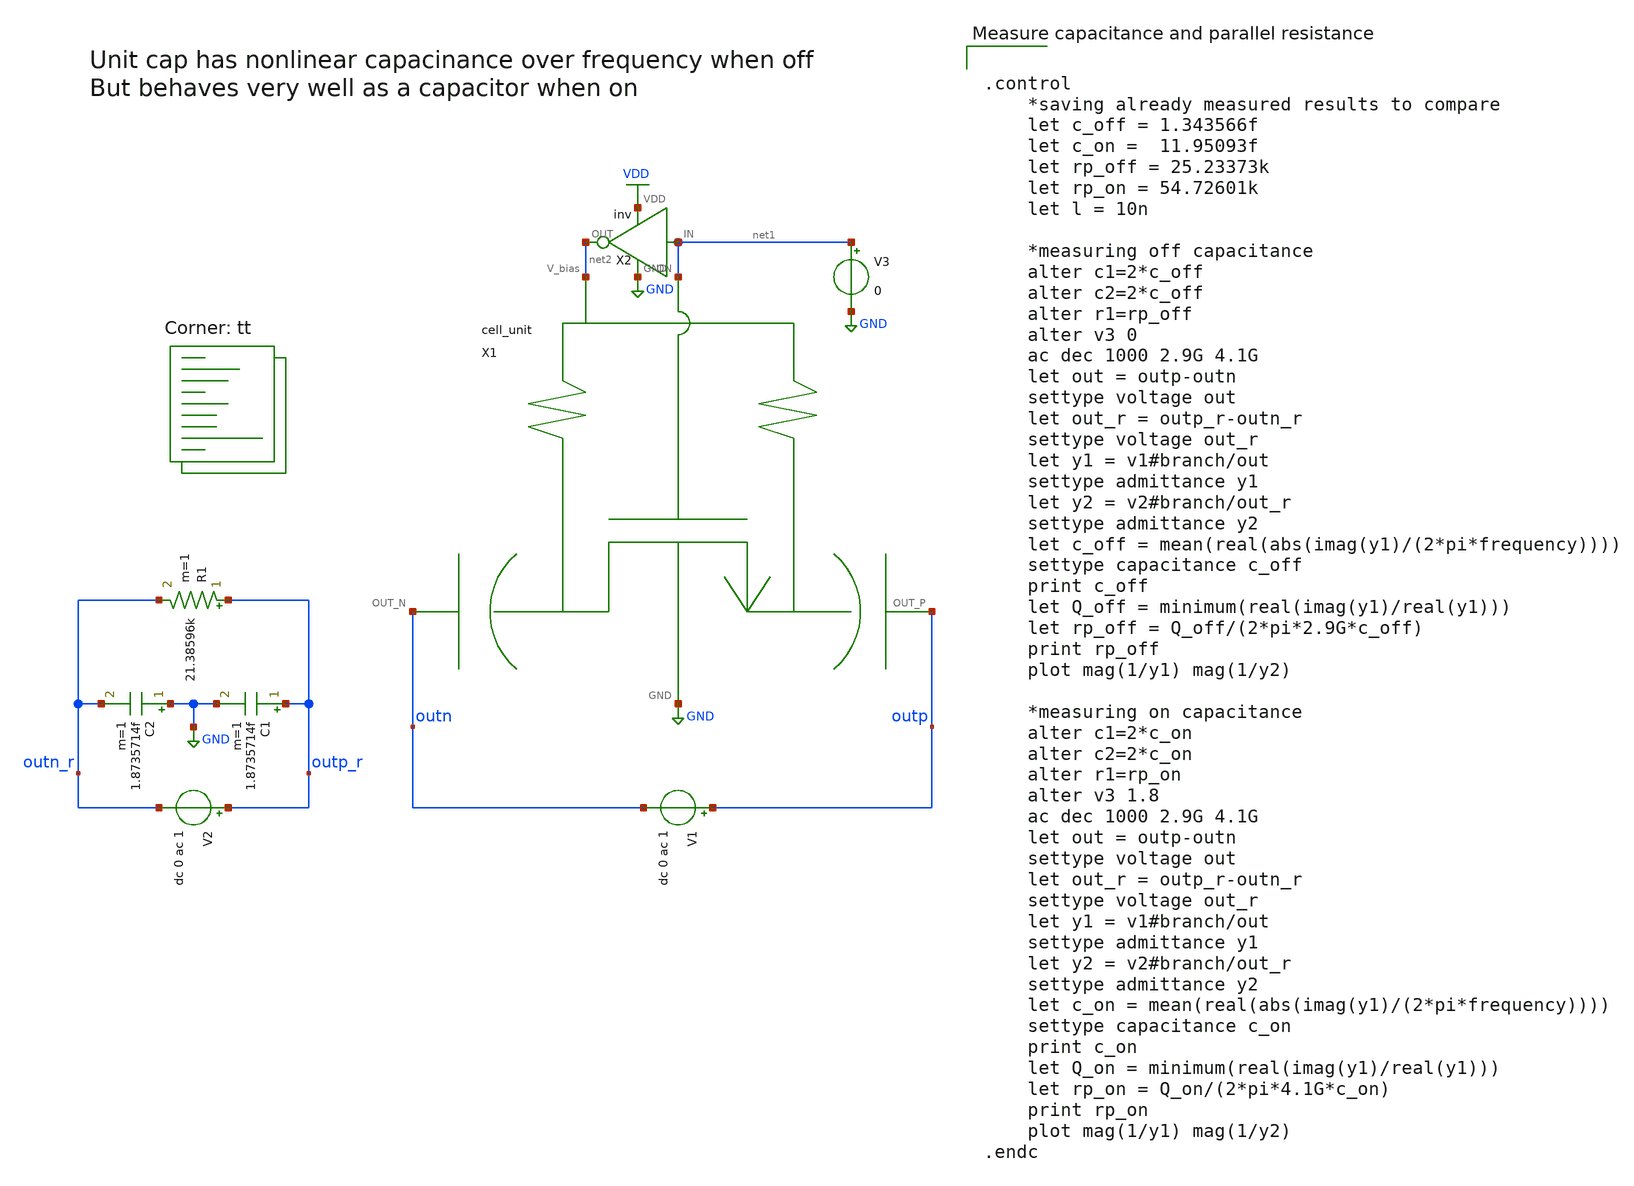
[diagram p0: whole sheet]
** sch_path: xschem/vco/testbenches/capbank/cell_unit_capacity_measurement_tb.sch
**.subckt cell_unit_capacity_measurement_tb
X1 net2 net1 outn GND outp cell_unit
X2 net1 net2 VDD GND inv
V3 net1 GND 0
V1 outp outn dc 0 ac 1
V2 outp_r outn_r dc 0 ac 1
C1 outp_r GND 1.8735714f m=1
C2 GND outn_r 1.8735714f m=1
R1 outp_r outn_r 21.38596k m=1
**** begin user architecture code
.lib $::SKYWATER_MODELS/sky130.lib.spice tt


.control
    *saving already measured results to compare
    let c_off = 1.343566f
    let c_on =  11.95093f
    let rp_off = 25.23373k
    let rp_on = 54.72601k
    let l = 10n

    *measuring off capacitance
    alter c1=2*c_off
    alter c2=2*c_off
    alter r1=rp_off
    alter v3 0
    ac dec 1000 2.9G 4.1G
    let out = outp-outn
    settype voltage out
    let out_r = outp_r-outn_r
    settype voltage out_r
    let y1 = v1#branch/out
    settype admittance y1
    let y2 = v2#branch/out_r
    settype admittance y2
    let c_off = mean(real(abs(imag(y1)/(2*pi*frequency))))
    settype capacitance c_off
    print c_off
    let Q_off = minimum(real(imag(y1)/real(y1)))
    let rp_off = Q_off/(2*pi*2.9G*c_off)
    print rp_off
    plot mag(1/y1) mag(1/y2)

    *measuring on capacitance
    alter c1=2*c_on
    alter c2=2*c_on
    alter r1=rp_on
    alter v3 1.8
    ac dec 1000 2.9G 4.1G
    let out = outp-outn
    settype voltage out
    let out_r = outp_r-outn_r
    settype voltage out_r
    let y1 = v1#branch/out
    settype admittance y1
    let y2 = v2#branch/out_r
    settype admittance y2
    let c_on = mean(real(abs(imag(y1)/(2*pi*frequency))))
    settype capacitance c_on
    print c_on
    let Q_on = minimum(real(imag(y1)/real(y1)))
    let rp_on = Q_on/(2*pi*4.1G*c_on)
    print rp_on
    plot mag(1/y1) mag(1/y2)
.endc


**** end user architecture code
**.ends
.GLOBAL GND
.GLOBAL VDD
.end
